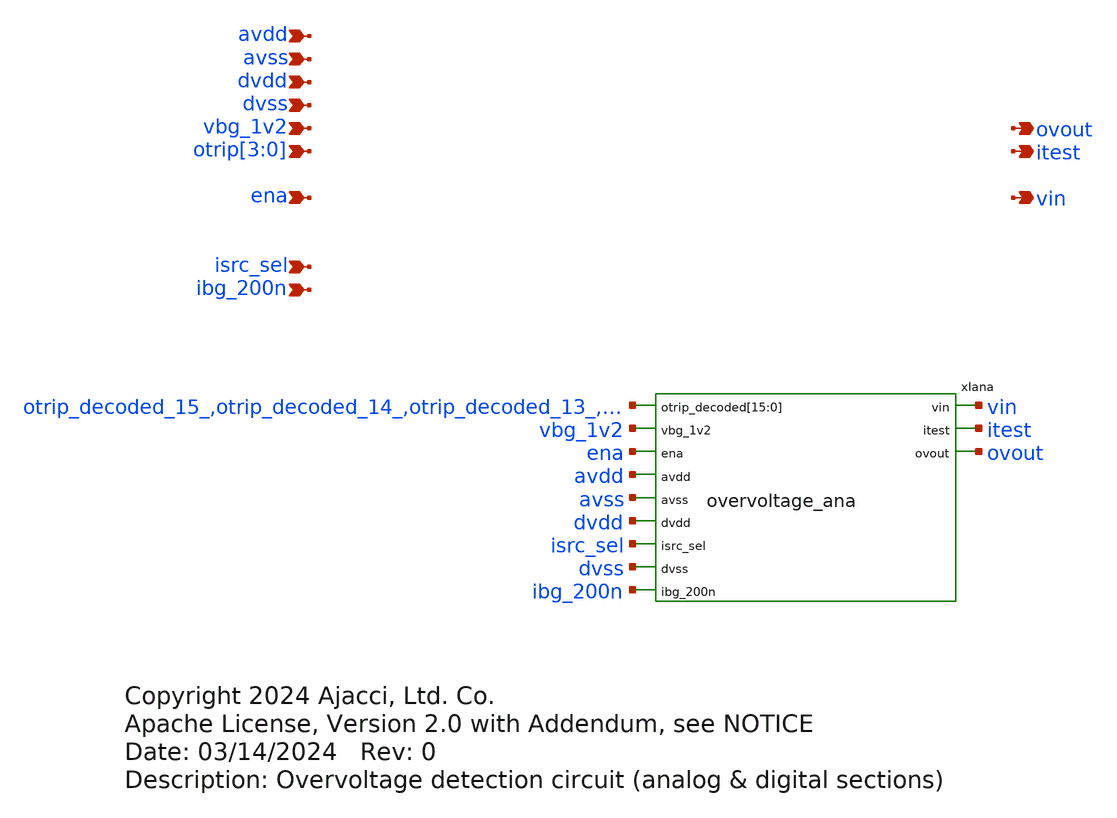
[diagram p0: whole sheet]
** sch_path: xschem/sky130_ajc_ip__overvoltage_sim.sch
* Copyright 2024 Ajacci, Ltd. Co.
* Apache License, Version 2.0 with Addendum, see NOTICE
**.subckt sky130_ajc_ip__overvoltage_sim avdd avss dvdd dvss vbg_1v2
*+ otrip[3],otrip[2],otrip[1],otrip[0] ena isrc_sel ibg_200n vin ovout itest
*.ipin avdd
*.ipin avss
*.ipin dvdd
*.ipin dvss
*.ipin vbg_1v2
*.ipin otrip[3],otrip[2],otrip[1],otrip[0]
*.ipin ena
*.ipin isrc_sel
*.ipin ibg_200n
*.opin vin
*.opin ovout
*.opin itest
xIana otrip_decoded_15_ otrip_decoded_14_ otrip_decoded_13_ otrip_decoded_12_ otrip_decoded_11_
+ otrip_decoded_10_ otrip_decoded_9_ otrip_decoded_8_ otrip_decoded_7_ otrip_decoded_6_ otrip_decoded_5_
+ otrip_decoded_4_ otrip_decoded_3_ otrip_decoded_2_ otrip_decoded_1_ otrip_decoded_0_ vbg_1v2 ena avdd avss dvdd
+ isrc_sel dvss vin itest ibg_200n ovout overvoltage_ana
**** begin user architecture code



*XSPICE CO-SIM netlist
.include overvoltage_dig.out.spice

r0 otrip[0] otrip0 1
r1 otrip[1] otrip1 1
r2 otrip[2] otrip2 1
r3 otrip[3] otrip3 1

xiovervoltage_dig dvss dvdd  otrip0 otrip1 otrip2 otrip3 otrip_decoded_0_  otrip_decoded_10_
+ otrip_decoded_11_ otrip_decoded_12_ otrip_decoded_13_ otrip_decoded_14_ otrip_decoded_15_ otrip_decoded_1_
+ otrip_decoded_2_ otrip_decoded_3_ otrip_decoded_4_ otrip_decoded_5_ otrip_decoded_6_ otrip_decoded_7_
+ otrip_decoded_8_ otrip_decoded_9_  overvoltage_dig



**** end user architecture code
**.ends
.end
